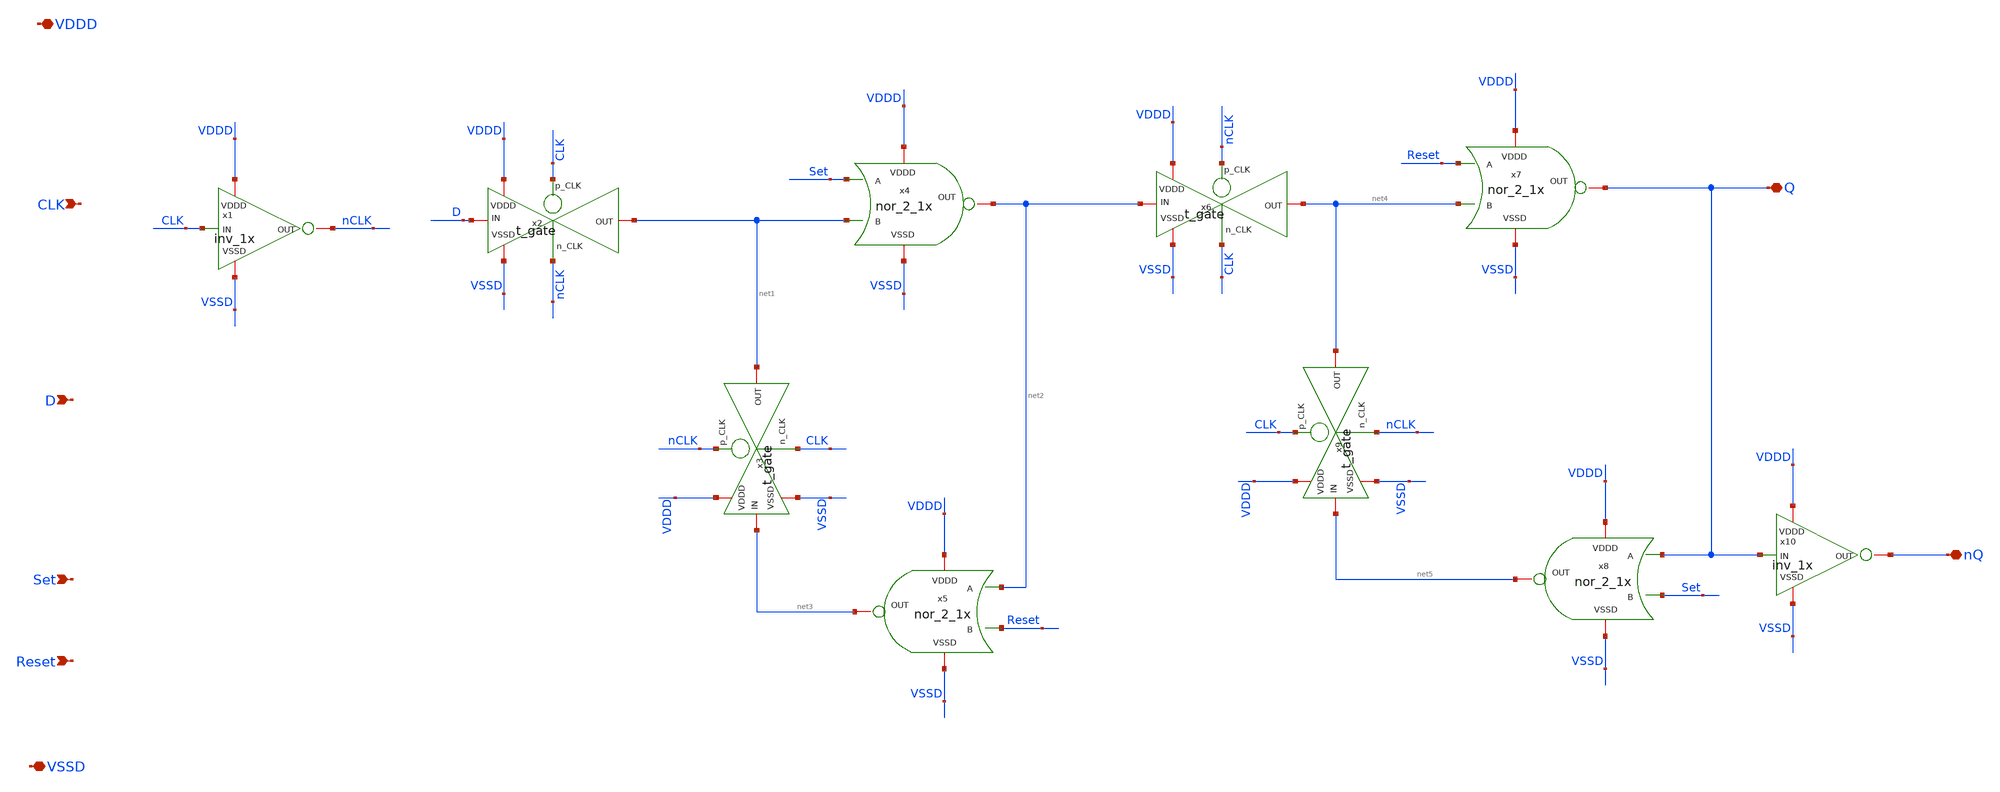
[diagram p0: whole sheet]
** sch_path: SAR_ADC/blocks/SAR_logic/D_reset_FF.sch
**.subckt D_reset_FF VDDD VSSD Q nQ CLK D Reset Set
*.iopin VDDD
*.iopin VSSD
*.iopin Q
*.iopin nQ
*.ipin CLK
*.ipin D
*.ipin Reset
*.ipin Set
x1 VDDD CLK nCLK VSSD inv_1x
x2 CLK VDDD D net1 VSSD nCLK t_gate
x3 nCLK VDDD net3 net1 VSSD CLK t_gate
x4 VDDD Set net2 net1 VSSD nor_2_1x
x5 VDDD net2 net3 Reset VSSD nor_2_1x
x6 nCLK VDDD net2 net4 VSSD CLK t_gate
x7 VDDD Reset Q net4 VSSD nor_2_1x
x8 VDDD Q net5 Set VSSD nor_2_1x
x9 CLK VDDD net5 net4 VSSD nCLK t_gate
x10 VDDD Q nQ VSSD inv_1x
**.ends
.end
